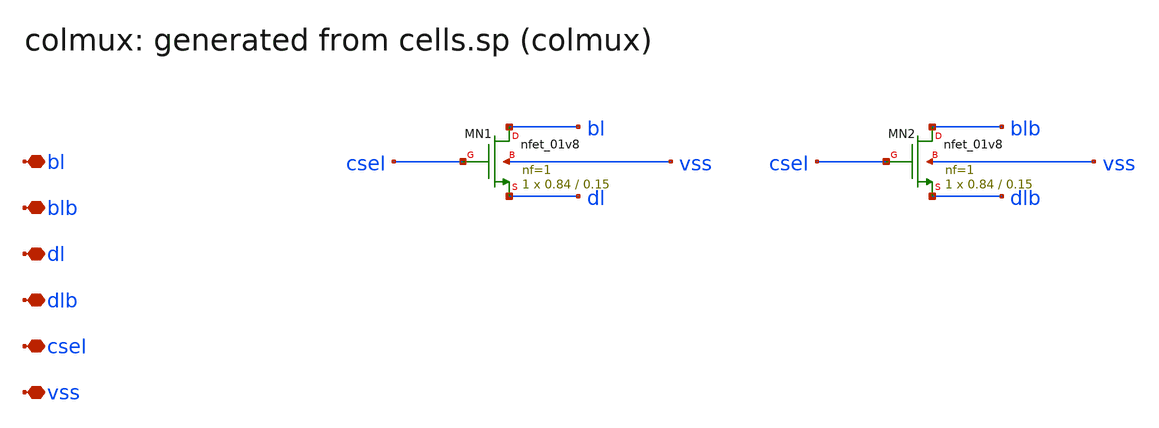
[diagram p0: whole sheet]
** sch_path: sram/xschem/colmux.sch
**.subckt colmux bl blb dl dlb csel vss
*.iopin bl
*.iopin blb
*.iopin dl
*.iopin dlb
*.iopin csel
*.iopin vss
XMN1 bl csel dl vss sky130_fd_pr__nfet_01v8 L=0.15 W=0.84 nf=1 ad='int((1 + 1)/2) * 0.84 / 1 * 0.29'
+ as='int((1 + 2)/2) * 0.84 / 1 * 0.29' pd='2*int((1 + 1)/2) * (0.84 / 1 + 0.29)' ps='2*int((1 + 2)/2) * (0.84 / 1 + 0.29)'
+ nrd='0.29 / 0.84 ' nrs='0.29 / 0.84 ' sa=0 sb=0 sd=0 mult=1 m=1
XMN2 blb csel dlb vss sky130_fd_pr__nfet_01v8 L=0.15 W=0.84 nf=1 ad='int((1 + 1)/2) * 0.84 / 1 * 0.29'
+ as='int((1 + 2)/2) * 0.84 / 1 * 0.29' pd='2*int((1 + 1)/2) * (0.84 / 1 + 0.29)' ps='2*int((1 + 2)/2) * (0.84 / 1 + 0.29)'
+ nrd='0.29 / 0.84 ' nrs='0.29 / 0.84 ' sa=0 sb=0 sd=0 mult=1 m=1
**.ends
.end
